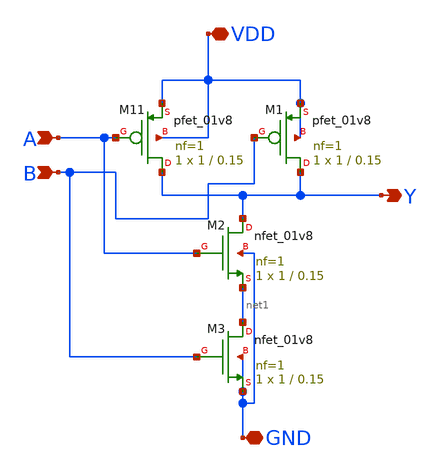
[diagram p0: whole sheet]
** sch_path: sar-adc/updated/Nand_Gate.sch
**.subckt Nand_Gate A B Y VDD GND
*.ipin A
*.ipin B
*.opin Y
*.iopin VDD
*.iopin GND
XM11 Y A VDD VDD sky130_fd_pr__pfet_01v8 L=0.15 W=1 nf=1 ad='int((nf+1)/2) * W/nf * 0.29' as='int((nf+2)/2) * W/nf * 0.29'
+ pd='2*int((nf+1)/2) * (W/nf + 0.29)' ps='2*int((nf+2)/2) * (W/nf + 0.29)' nrd='0.29 / W' nrs='0.29 / W'
+ sa=0 sb=0 sd=0 mult=1 m=1
XM1 Y B VDD VDD sky130_fd_pr__pfet_01v8 L=0.15 W=1 nf=1 ad='int((nf+1)/2) * W/nf * 0.29' as='int((nf+2)/2) * W/nf * 0.29'
+ pd='2*int((nf+1)/2) * (W/nf + 0.29)' ps='2*int((nf+2)/2) * (W/nf + 0.29)' nrd='0.29 / W' nrs='0.29 / W'
+ sa=0 sb=0 sd=0 mult=1 m=1
XM2 Y A net1 GND sky130_fd_pr__nfet_01v8 L=0.15 W=1 nf=1 ad='int((1 + 1)/2) * 1 / 1 * 0.29' as='int((1 + 2)/2) * 1 / 1 * 0.29'
+ pd='2*int((1 + 1)/2) * (1 / 1 + 0.29)' ps='2*int((1 + 2)/2) * (1 / 1 + 0.29)' nrd='0.29 / 1 ' nrs='0.29 / 1 '
+ sa=0 sb=0 sd=0 mult=1 m=1
XM3 net1 B GND GND sky130_fd_pr__nfet_01v8 L=0.15 W=1 nf=1 ad='int((1 + 1)/2) * 1 / 1 * 0.29' as='int((1 + 2)/2) * 1 / 1 * 0.29'
+ pd='2*int((1 + 1)/2) * (1 / 1 + 0.29)' ps='2*int((1 + 2)/2) * (1 / 1 + 0.29)' nrd='0.29 / 1 ' nrs='0.29 / 1 '
+ sa=0 sb=0 sd=0 mult=1 m=1
**.ends
.end
